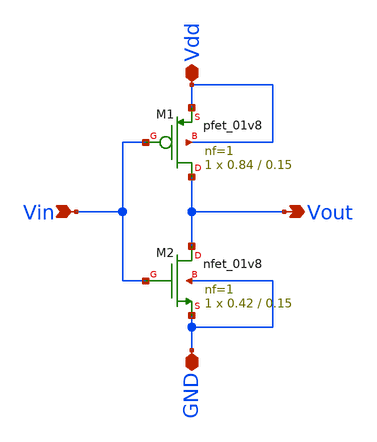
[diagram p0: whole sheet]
** sch_path: xschem_project/inverter/inverter.sch
**.subckt inverter Vin Vout Vdd GND
*.ipin Vin
*.opin Vout
*.iopin Vdd
*.iopin GND
XM1 Vout Vin Vdd Vdd sky130_fd_pr__pfet_01v8 L=0.15 W=0.84 nf=1 ad='int((1 + 1)/2) * 0.84 / 1 * 0.29'
+ as='int((1 + 2)/2) * 0.84 / 1 * 0.29' pd='2*int((1 + 1)/2) * (0.84 / 1 + 0.29)' ps='2*int((1 + 2)/2) * (0.84 / 1 + 0.29)'
+ nrd='0.29 / 0.84 ' nrs='0.29 / 0.84 ' sa=0 sb=0 sd=0 mult=1 m=1
XM2 Vout Vin GND GND sky130_fd_pr__nfet_01v8 L=0.15 W=0.42 nf=1 ad='int((1 + 1)/2) * 0.42 / 1 * 0.29'
+ as='int((1 + 2)/2) * 0.42 / 1 * 0.29' pd='2*int((1 + 1)/2) * (0.42 / 1 + 0.29)' ps='2*int((1 + 2)/2) * (0.42 / 1 + 0.29)'
+ nrd='0.29 / 0.42 ' nrs='0.29 / 0.42 ' sa=0 sb=0 sd=0 mult=1 m=1
**.ends
.end
